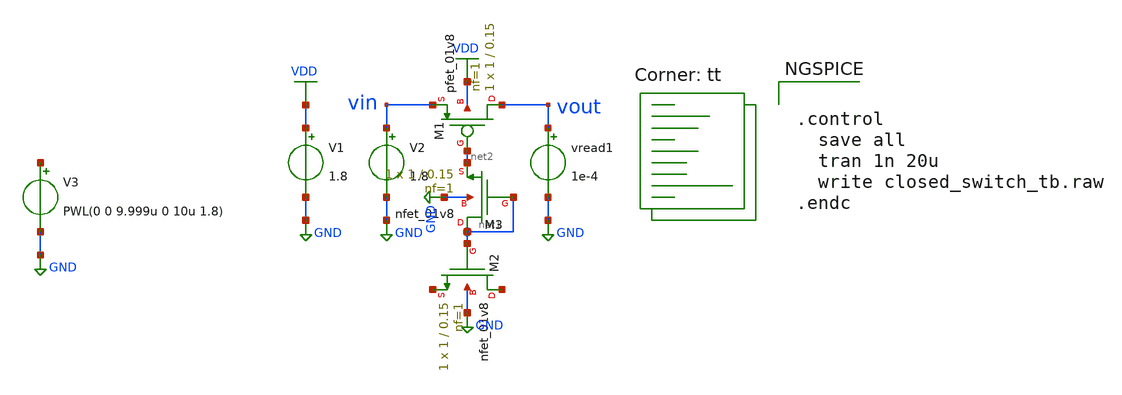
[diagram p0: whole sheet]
** sch_path: switch/closed_switch_tb.sch
**.subckt closed_switch_tb
V1 VDD GND 1.8
V2 vin GND 1.8
XM1 vout net2 vin VDD sky130_fd_pr__pfet_01v8 L=0.15 W=1 nf=1 ad='int((nf+1)/2) * W/nf * 0.29' as='int((nf+2)/2) * W/nf * 0.29'
+ pd='2*int((nf+1)/2) * (W/nf + 0.29)' ps='2*int((nf+2)/2) * (W/nf + 0.29)' nrd='0.29 / W' nrs='0.29 / W'
+ sa=0 sb=0 sd=0 mult=1 m=1
V3 net3 GND PWL(0 0 9.999u 0 10u 1.8)
vread1 vout GND 1e-4
XM2 net4 net1 net5 GND sky130_fd_pr__nfet_01v8 L=0.15 W=1 nf=1 ad='int((nf+1)/2) * W/nf * 0.29' as='int((nf+2)/2) * W/nf * 0.29'
+ pd='2*int((nf+1)/2) * (W/nf + 0.29)' ps='2*int((nf+2)/2) * (W/nf + 0.29)' nrd='0.29 / W' nrs='0.29 / W'
+ sa=0 sb=0 sd=0 mult=1 m=1
XM3 net1 net1 net2 GND sky130_fd_pr__nfet_01v8 L=0.15 W=1 nf=1 ad='int((nf+1)/2) * W/nf * 0.29' as='int((nf+2)/2) * W/nf * 0.29'
+ pd='2*int((nf+1)/2) * (W/nf + 0.29)' ps='2*int((nf+2)/2) * (W/nf + 0.29)' nrd='0.29 / W' nrs='0.29 / W'
+ sa=0 sb=0 sd=0 mult=1 m=1
**** begin user architecture code
.lib $::SKYWATER_MODELS/sky130.lib.spice tt


.control
  save all
  tran 1n 20u
  write closed_switch_tb.raw
.endc


**** end user architecture code
**.ends
.GLOBAL VDD
.GLOBAL GND
.end
